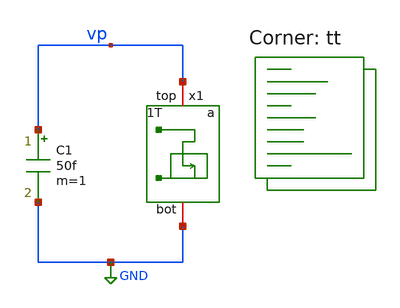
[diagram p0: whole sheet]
** sch_path: xschem/tb/dschr_nwk_type_a_tb.sch
**.subckt dschr_nwk_type_a_tb
C1 vp GND 50f m=1
x1 vp GND dschr_nwk_type_a L=0.15 W=0.5
**** begin user architecture code
.lib $::SKYWATER_MODELS/sky130.lib.spice tt


.include $::netlist_dir/ctrl_sims.spice


**** end user architecture code
**.ends
.GLOBAL GND
.end
